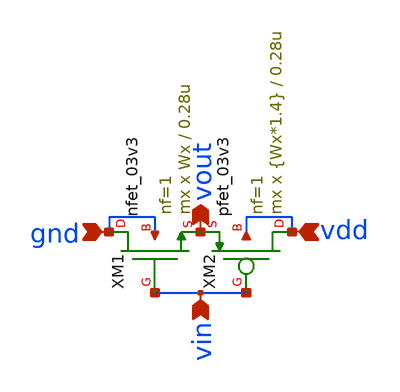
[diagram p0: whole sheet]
** sch_path: xschem/designs/inv.sch
**.subckt inv gnd vdd vin vout
*.ipin gnd
*.ipin vdd
*.ipin vin
*.opin vout
XM1 gnd vin vout gnd nfet_03v3 L=0.28u W=Wx nf=1 ad='int((nf+1)/2) * W/nf * 0.18u' as='int((nf+2)/2) * W/nf * 0.18u'
+ pd='2*int((nf+1)/2) * (W/nf + 0.18u)' ps='2*int((nf+2)/2) * (W/nf + 0.18u)' nrd='0.18u / W' nrs='0.18u / W'
+ sa=0 sb=0 sd=0 m=mx
XM2 vdd vin vout vdd pfet_03v3 L=0.28u W={Wx*1.4} nf=1 ad='int((nf+1)/2) * W/nf * 0.18u' as='int((nf+2)/2) * W/nf * 0.18u'
+ pd='2*int((nf+1)/2) * (W/nf + 0.18u)' ps='2*int((nf+2)/2) * (W/nf + 0.18u)' nrd='0.18u / W' nrs='0.18u / W'
+ sa=0 sb=0 sd=0 m=mx
**** begin user architecture code

.include /foss/pdks/gf180mcuC/libs.tech/ngspice/design.ngspice
.lib /foss/pdks/gf180mcuC/libs.tech/ngspice/sm141064.ngspice typical

**** end user architecture code
**.ends
.end
